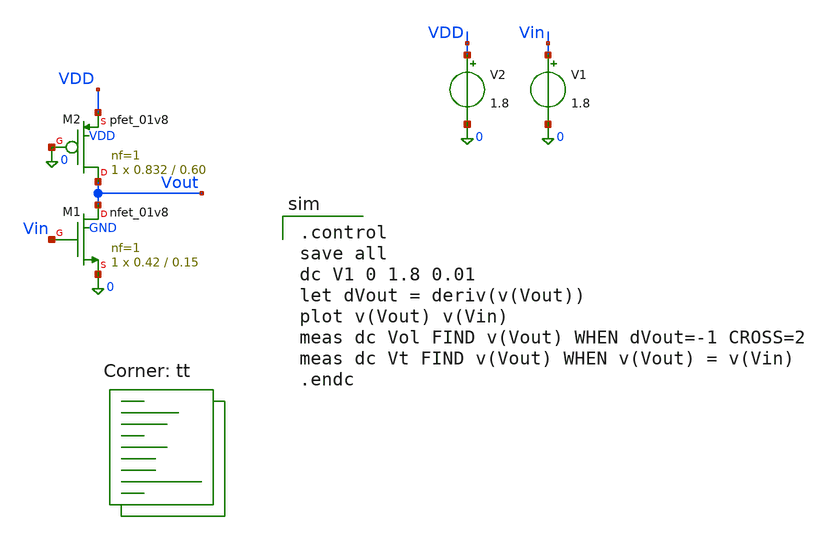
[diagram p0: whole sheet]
** sch_path: tutorial-2/source/q2a.sch
**.subckt q2a
V1 Vin 0 1.8
XM1 Vout Vin 0 GND sky130_fd_pr__nfet_01v8 L=0.15 W=0.42 nf=1 ad='int((nf+1)/2) * W/nf * 0.29' as='int((nf+2)/2) * W/nf * 0.29'
+ pd='2*int((nf+1)/2) * (W/nf + 0.29)' ps='2*int((nf+2)/2) * (W/nf + 0.29)' nrd='0.29 / W' nrs='0.29 / W'
+ sa=0 sb=0 sd=0 mult=1 m=1
XM2 Vout 0 VDD VDD sky130_fd_pr__pfet_01v8 L=0.60 W=0.832 nf=1 ad='int((nf+1)/2) * W/nf * 0.29' as='int((nf+2)/2) * W/nf * 0.29'
+ pd='2*int((nf+1)/2) * (W/nf + 0.29)' ps='2*int((nf+2)/2) * (W/nf + 0.29)' nrd='0.29 / W' nrs='0.29 / W'
+ sa=0 sb=0 sd=0 mult=1 m=1
V2 VDD 0 1.8
**** begin user architecture code
.lib $::SKYWATER_MODELS/sky130.lib.spice tt

.control
save all
dc V1 0 1.8 0.01
let dVout = deriv(v(Vout))
plot v(Vout) v(Vin)
meas dc Vol FIND v(Vout) WHEN dVout=-1 CROSS=2
meas dc Vt FIND v(Vout) WHEN v(Vout) = v(Vin)
.endc

**** end user architecture code
**.ends
.end
